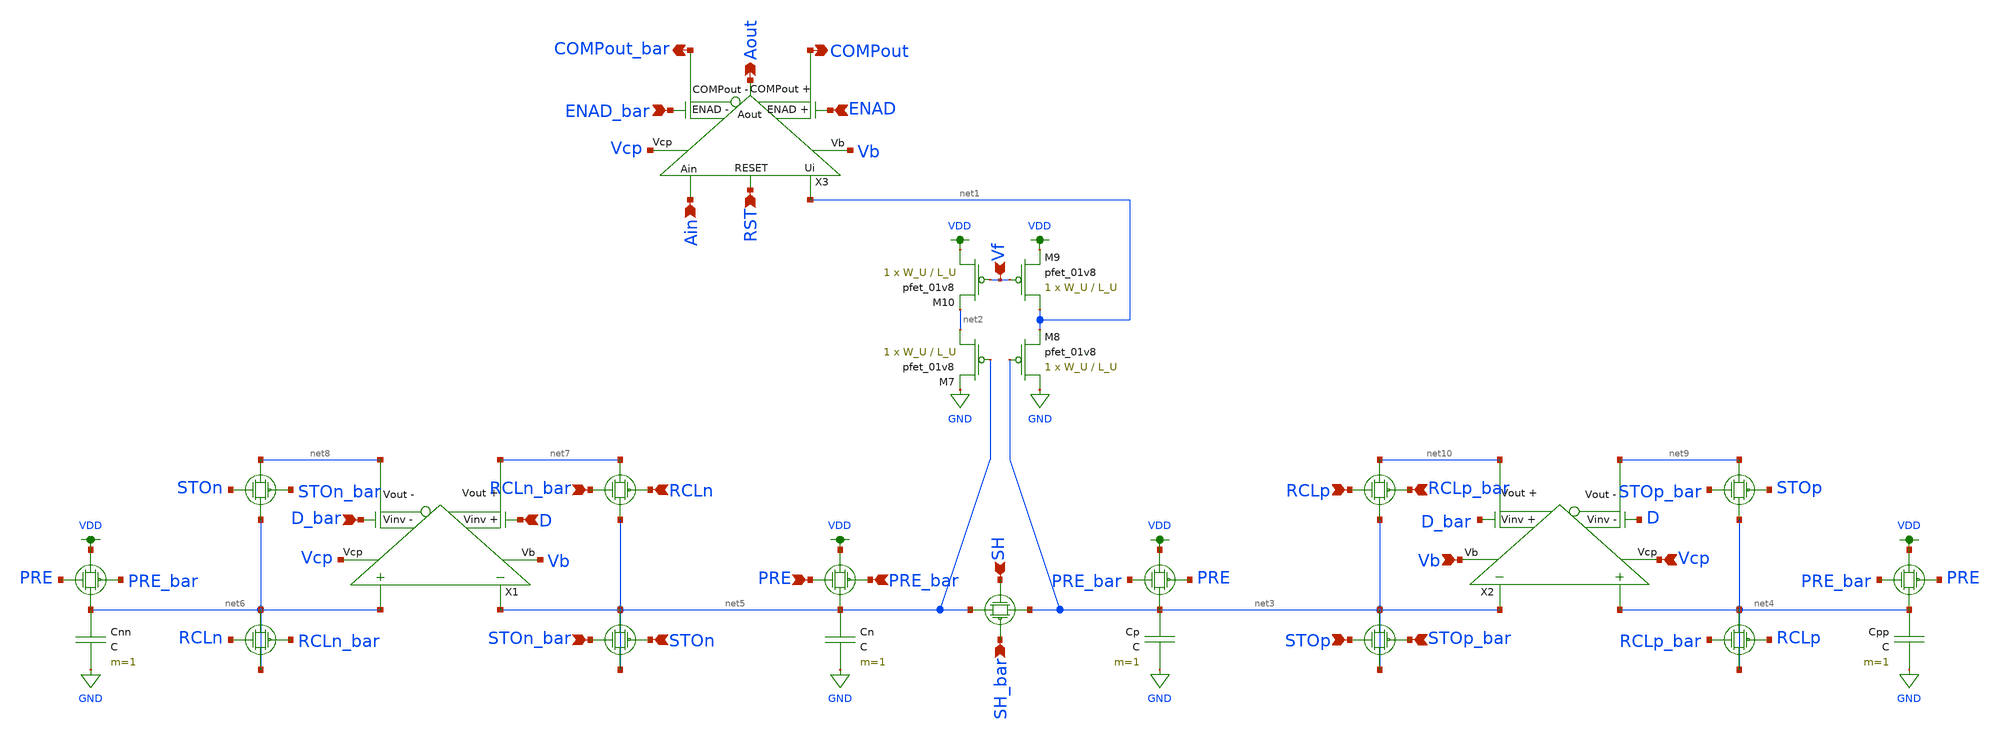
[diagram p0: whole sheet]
** sch_path: schematics/ada_converter.sch
**.subckt ada_converter RCLp STOp RCLp_bar STOp_bar SH SH_bar Vb Vcp RCLn STOn RCLn_bar STOn_bar RST
*+ Ain Aout COMPout_bar COMPout ENAD ENAD_bar Vf PRE_bar PRE D_bar D
*.ipin RCLp
*.ipin STOp
*.ipin RCLp_bar
*.ipin STOp_bar
*.ipin SH
*.ipin SH_bar
*.ipin Vb
*.ipin Vcp
*.ipin RCLn
*.ipin STOn
*.ipin RCLn_bar
*.ipin STOn_bar
*.ipin RST
*.ipin Ain
*.opin Aout
*.opin COMPout_bar
*.opin COMPout
*.ipin ENAD
*.ipin ENAD_bar
*.ipin Vf
*.ipin PRE_bar
*.ipin PRE
*.ipin D_bar
*.ipin D
X1 D_bar net8 net7 Vcp Vb net5 net6 D ota
X2 D net9 net10 Vcp Vb net3 net4 D_bar ota
X3 ENAD_bar COMPout_bar COMPout Vb net1 Ain ENAD Aout Vcp RST comp_pretty
Cp net3 GND C m=1
XM7 net2 net5 GND VDD sky130_fd_pr__pfet_01v8 L=L_U W=W_U nf=1 ad='int((nf+1)/2) * W/nf * 0.29' as='int((nf+2)/2) * W/nf * 0.29'
+ pd='2*int((nf+1)/2) * (W/nf + 0.29)' ps='2*int((nf+2)/2) * (W/nf + 0.29)' nrd='0.29 / W' nrs='0.29 / W'
+ sa=0 sb=0 sd=0 mult=1 m=1
XM8 GND net3 net1 VDD sky130_fd_pr__pfet_01v8 L=L_U W=W_U nf=1 ad='int((nf+1)/2) * W/nf * 0.29' as='int((nf+2)/2) * W/nf * 0.29'
+ pd='2*int((nf+1)/2) * (W/nf + 0.29)' ps='2*int((nf+2)/2) * (W/nf + 0.29)' nrd='0.29 / W' nrs='0.29 / W'
+ sa=0 sb=0 sd=0 mult=1 m=1
XM9 net1 Vf VDD VDD sky130_fd_pr__pfet_01v8 L=L_U W=W_U nf=1 ad='int((nf+1)/2) * W/nf * 0.29' as='int((nf+2)/2) * W/nf * 0.29'
+ pd='2*int((nf+1)/2) * (W/nf + 0.29)' ps='2*int((nf+2)/2) * (W/nf + 0.29)' nrd='0.29 / W' nrs='0.29 / W'
+ sa=0 sb=0 sd=0 mult=1 m=1
XM10 VDD Vf net2 VDD sky130_fd_pr__pfet_01v8 L=L_U W=W_U nf=1 ad='int((nf+1)/2) * W/nf * 0.29' as='int((nf+2)/2) * W/nf * 0.29'
+ pd='2*int((nf+1)/2) * (W/nf + 0.29)' ps='2*int((nf+2)/2) * (W/nf + 0.29)' nrd='0.29 / W' nrs='0.29 / W'
+ sa=0 sb=0 sd=0 mult=1 m=1
Cpp net4 GND C m=1
Cn net5 GND C m=1
Cnn net6 GND C m=1
**.ends

* expanding   symbol:  ./ota.sym # of pins=8
** sym_path: schematics/ota.sym
** sch_path: schematics/ota.sch
.subckt ota Vinv_n Vout_n Vout_p Vcp Vb Vin_n Vin_p Vinv_p
*.ipin Vin_n
*.ipin Vin_p
*.opin Vout_n
*.opin Vout_p
*.ipin Vcp
*.ipin Vb
*.ipin Vinv_p
*.ipin Vinv_n
XM18 net3 net3 VDD VDD sky130_fd_pr__pfet_01v8 L=L_U W=W_U nf=1 ad='int((nf+1)/2) * W/nf * 0.29' as='int((nf+2)/2) * W/nf * 0.29'
+ pd='2*int((nf+1)/2) * (W/nf + 0.29)' ps='2*int((nf+2)/2) * (W/nf + 0.29)' nrd='0.29 / W' nrs='0.29 / W'
+ sa=0 sb=0 sd=0 mult=1 m=1
XM19 net4 Vin_n net1 GND sky130_fd_pr__nfet_01v8 L=L_U W=W_U nf=1 ad='int((nf+1)/2) * W/nf * 0.29' as='int((nf+2)/2) * W/nf * 0.29'
+ pd='2*int((nf+1)/2) * (W/nf + 0.29)' ps='2*int((nf+2)/2) * (W/nf + 0.29)' nrd='0.29 / W' nrs='0.29 / W'
+ sa=0 sb=0 sd=0 mult=1 m=1
XM20 net3 Vin_p net1 GND sky130_fd_pr__nfet_01v8 L=L_U W=W_U nf=1 ad='int((nf+1)/2) * W/nf * 0.29' as='int((nf+2)/2) * W/nf * 0.29'
+ pd='2*int((nf+1)/2) * (W/nf + 0.29)' ps='2*int((nf+2)/2) * (W/nf + 0.29)' nrd='0.29 / W' nrs='0.29 / W'
+ sa=0 sb=0 sd=0 mult=1 m=1
XM21 net1 Vb GND GND sky130_fd_pr__nfet_01v8 L=L_U W=W_U nf=1 ad='int((nf+1)/2) * W/nf * 0.29' as='int((nf+2)/2) * W/nf * 0.29'
+ pd='2*int((nf+1)/2) * (W/nf + 0.29)' ps='2*int((nf+2)/2) * (W/nf + 0.29)' nrd='0.29 / W' nrs='0.29 / W'
+ sa=0 sb=0 sd=0 mult=1 m=1
XM22 net4 net4 VDD VDD sky130_fd_pr__pfet_01v8 L=L_U W=W_U nf=1 ad='int((nf+1)/2) * W/nf * 0.29' as='int((nf+2)/2) * W/nf * 0.29'
+ pd='2*int((nf+1)/2) * (W/nf + 0.29)' ps='2*int((nf+2)/2) * (W/nf + 0.29)' nrd='0.29 / W' nrs='0.29 / W'
+ sa=0 sb=0 sd=0 mult=1 m=1
XM23 net8 net3 VDD VDD sky130_fd_pr__pfet_01v8 L=L_U W=W_U nf=1 ad='int((nf+1)/2) * W/nf * 0.29' as='int((nf+2)/2) * W/nf * 0.29'
+ pd='2*int((nf+1)/2) * (W/nf + 0.29)' ps='2*int((nf+2)/2) * (W/nf + 0.29)' nrd='0.29 / W' nrs='0.29 / W'
+ sa=0 sb=0 sd=0 mult=1 m=1
XM24 net9 net4 VDD VDD sky130_fd_pr__pfet_01v8 L=L_U W=W_U nf=1 ad='int((nf+1)/2) * W/nf * 0.29' as='int((nf+2)/2) * W/nf * 0.29'
+ pd='2*int((nf+1)/2) * (W/nf + 0.29)' ps='2*int((nf+2)/2) * (W/nf + 0.29)' nrd='0.29 / W' nrs='0.29 / W'
+ sa=0 sb=0 sd=0 mult=1 m=1
XM25 net9 Vcp Vout_n VDD sky130_fd_pr__pfet_01v8 L=L_U W=W_U nf=1 ad='int((nf+1)/2) * W/nf * 0.29' as='int((nf+2)/2) * W/nf * 0.29'
+ pd='2*int((nf+1)/2) * (W/nf + 0.29)' ps='2*int((nf+2)/2) * (W/nf + 0.29)' nrd='0.29 / W' nrs='0.29 / W'
+ sa=0 sb=0 sd=0 mult=1 m=1
XM26 Vout_p Vcp net8 VDD sky130_fd_pr__pfet_01v8 L=L_U W=W_U nf=1 ad='int((nf+1)/2) * W/nf * 0.29' as='int((nf+2)/2) * W/nf * 0.29'
+ pd='2*int((nf+1)/2) * (W/nf + 0.29)' ps='2*int((nf+2)/2) * (W/nf + 0.29)' nrd='0.29 / W' nrs='0.29 / W'
+ sa=0 sb=0 sd=0 mult=1 m=1
XM27 Vout_p net7 net5 GND sky130_fd_pr__nfet_01v8 L=L_U W=W_U nf=1 ad='int((nf+1)/2) * W/nf * 0.29' as='int((nf+2)/2) * W/nf * 0.29'
+ pd='2*int((nf+1)/2) * (W/nf + 0.29)' ps='2*int((nf+2)/2) * (W/nf + 0.29)' nrd='0.29 / W' nrs='0.29 / W'
+ sa=0 sb=0 sd=0 mult=1 m=1
XM28 Vout_n net7 net2 GND sky130_fd_pr__nfet_01v8 L=L_U W=W_U nf=1 ad='int((nf+1)/2) * W/nf * 0.29' as='int((nf+2)/2) * W/nf * 0.29'
+ pd='2*int((nf+1)/2) * (W/nf + 0.29)' ps='2*int((nf+2)/2) * (W/nf + 0.29)' nrd='0.29 / W' nrs='0.29 / W'
+ sa=0 sb=0 sd=0 mult=1 m=1
XM29 net5 net6 GND GND sky130_fd_pr__nfet_01v8 L=L_U W=W_U nf=1 ad='int((nf+1)/2) * W/nf * 0.29' as='int((nf+2)/2) * W/nf * 0.29'
+ pd='2*int((nf+1)/2) * (W/nf + 0.29)' ps='2*int((nf+2)/2) * (W/nf + 0.29)' nrd='0.29 / W' nrs='0.29 / W'
+ sa=0 sb=0 sd=0 mult=1 m=1
XM30 net5 Vinv_p net6 GND sky130_fd_pr__nfet_01v8 L=L_U W=W_U nf=1 ad='int((nf+1)/2) * W/nf * 0.29' as='int((nf+2)/2) * W/nf * 0.29'
+ pd='2*int((nf+1)/2) * (W/nf + 0.29)' ps='2*int((nf+2)/2) * (W/nf + 0.29)' nrd='0.29 / W' nrs='0.29 / W'
+ sa=0 sb=0 sd=0 mult=1 m=1
XM31 Vout_p Vinv_p net7 GND sky130_fd_pr__nfet_01v8 L=L_U W=W_U nf=1 ad='int((nf+1)/2) * W/nf * 0.29'
+ as='int((nf+2)/2) * W/nf * 0.29' pd='2*int((nf+1)/2) * (W/nf + 0.29)' ps='2*int((nf+2)/2) * (W/nf + 0.29)'
+ nrd='0.29 / W' nrs='0.29 / W' sa=0 sb=0 sd=0 mult=1 m=1
XM32 net2 net6 GND GND sky130_fd_pr__nfet_01v8 L=L_U W=W_U nf=1 ad='int((nf+1)/2) * W/nf * 0.29' as='int((nf+2)/2) * W/nf * 0.29'
+ pd='2*int((nf+1)/2) * (W/nf + 0.29)' ps='2*int((nf+2)/2) * (W/nf + 0.29)' nrd='0.29 / W' nrs='0.29 / W'
+ sa=0 sb=0 sd=0 mult=1 m=1
XM33 Vout_n Vinv_n net7 GND sky130_fd_pr__nfet_01v8 L=L_U W=W_U nf=1 ad='int((nf+1)/2) * W/nf * 0.29'
+ as='int((nf+2)/2) * W/nf * 0.29' pd='2*int((nf+1)/2) * (W/nf + 0.29)' ps='2*int((nf+2)/2) * (W/nf + 0.29)'
+ nrd='0.29 / W' nrs='0.29 / W' sa=0 sb=0 sd=0 mult=1 m=1
XM34 net2 Vinv_n net6 GND sky130_fd_pr__nfet_01v8 L=L_U W=W_U nf=1 ad='int((nf+1)/2) * W/nf * 0.29' as='int((nf+2)/2) * W/nf * 0.29'
+ pd='2*int((nf+1)/2) * (W/nf + 0.29)' ps='2*int((nf+2)/2) * (W/nf + 0.29)' nrd='0.29 / W' nrs='0.29 / W'
+ sa=0 sb=0 sd=0 mult=1 m=1
.ends


* expanding   symbol:  ./comp_pretty.sym # of pins=10
** sym_path: schematics/comp_pretty.sym
** sch_path: schematics/comp_pretty.sch
.subckt comp_pretty ENAD_n COMPout_n COMPout_p Vb Ui Ain ENAD_p Aout Vcp RST
*.ipin Ain
*.ipin Vcp
*.ipin Vb
*.opin Aout
*.opin COMPout_n
*.opin COMPout_p
*.ipin ENAD_n
*.ipin RST
*.ipin Ui
*.ipin ENAD_p
XM1 net1 net1 VDD VDD sky130_fd_pr__pfet_01v8 L=L_U W=W_U nf=1 ad='int((nf+1)/2) * W/nf * 0.29' as='int((nf+2)/2) * W/nf * 0.29'
+ pd='2*int((nf+1)/2) * (W/nf + 0.29)' ps='2*int((nf+2)/2) * (W/nf + 0.29)' nrd='0.29 / W' nrs='0.29 / W'
+ sa=0 sb=0 sd=0 mult=1 m=1
XM2 net2 Ain net5 GND sky130_fd_pr__nfet_01v8 L=L_U W=W_U nf=1 ad='int((nf+1)/2) * W/nf * 0.29' as='int((nf+2)/2) * W/nf * 0.29'
+ pd='2*int((nf+1)/2) * (W/nf + 0.29)' ps='2*int((nf+2)/2) * (W/nf + 0.29)' nrd='0.29 / W' nrs='0.29 / W'
+ sa=0 sb=0 sd=0 mult=1 m=1
XM3 net1 Ui net5 GND sky130_fd_pr__nfet_01v8 L=L_U W=W_U nf=1 ad='int((nf+1)/2) * W/nf * 0.29' as='int((nf+2)/2) * W/nf * 0.29'
+ pd='2*int((nf+1)/2) * (W/nf + 0.29)' ps='2*int((nf+2)/2) * (W/nf + 0.29)' nrd='0.29 / W' nrs='0.29 / W'
+ sa=0 sb=0 sd=0 mult=1 m=1
XM4 net5 Vb GND GND sky130_fd_pr__nfet_01v8 L=L_U W=W_U nf=1 ad='int((nf+1)/2) * W/nf * 0.29' as='int((nf+2)/2) * W/nf * 0.29'
+ pd='2*int((nf+1)/2) * (W/nf + 0.29)' ps='2*int((nf+2)/2) * (W/nf + 0.29)' nrd='0.29 / W' nrs='0.29 / W'
+ sa=0 sb=0 sd=0 mult=1 m=1
XM5 net2 net2 VDD VDD sky130_fd_pr__pfet_01v8 L=L_U W=W_U nf=1 ad='int((nf+1)/2) * W/nf * 0.29' as='int((nf+2)/2) * W/nf * 0.29'
+ pd='2*int((nf+1)/2) * (W/nf + 0.29)' ps='2*int((nf+2)/2) * (W/nf + 0.29)' nrd='0.29 / W' nrs='0.29 / W'
+ sa=0 sb=0 sd=0 mult=1 m=1
XM6 net8 net1 VDD VDD sky130_fd_pr__pfet_01v8 L=L_U W=W_U nf=1 ad='int((nf+1)/2) * W/nf * 0.29' as='int((nf+2)/2) * W/nf * 0.29'
+ pd='2*int((nf+1)/2) * (W/nf + 0.29)' ps='2*int((nf+2)/2) * (W/nf + 0.29)' nrd='0.29 / W' nrs='0.29 / W'
+ sa=0 sb=0 sd=0 mult=1 m=1
XM7 net9 net2 VDD VDD sky130_fd_pr__pfet_01v8 L=L_U W=W_U nf=1 ad='int((nf+1)/2) * W/nf * 0.29' as='int((nf+2)/2) * W/nf * 0.29'
+ pd='2*int((nf+1)/2) * (W/nf + 0.29)' ps='2*int((nf+2)/2) * (W/nf + 0.29)' nrd='0.29 / W' nrs='0.29 / W'
+ sa=0 sb=0 sd=0 mult=1 m=1
XM8 net9 Vcp COMPout_p VDD sky130_fd_pr__pfet_01v8 L=L_U W=W_U nf=1 ad='int((nf+1)/2) * W/nf * 0.29'
+ as='int((nf+2)/2) * W/nf * 0.29' pd='2*int((nf+1)/2) * (W/nf + 0.29)' ps='2*int((nf+2)/2) * (W/nf + 0.29)'
+ nrd='0.29 / W' nrs='0.29 / W' sa=0 sb=0 sd=0 mult=1 m=1
XM9 COMPout_n Vcp net8 VDD sky130_fd_pr__pfet_01v8 L=L_U W=W_U nf=1 ad='int((nf+1)/2) * W/nf * 0.29'
+ as='int((nf+2)/2) * W/nf * 0.29' pd='2*int((nf+1)/2) * (W/nf + 0.29)' ps='2*int((nf+2)/2) * (W/nf + 0.29)'
+ nrd='0.29 / W' nrs='0.29 / W' sa=0 sb=0 sd=0 mult=1 m=1
XM10 net1 Vb GND GND sky130_fd_pr__nfet_01v8 L=L_U W=W_U nf=1 ad='int((nf+1)/2) * W/nf * 0.29' as='int((nf+2)/2) * W/nf * 0.29'
+ pd='2*int((nf+1)/2) * (W/nf + 0.29)' ps='2*int((nf+2)/2) * (W/nf + 0.29)' nrd='0.29 / W' nrs='0.29 / W'
+ sa=0 sb=0 sd=0 mult=1 m=1
XM11 net2 Vb GND GND sky130_fd_pr__nfet_01v8 L=L_U W=W_U nf=1 ad='int((nf+1)/2) * W/nf * 0.29' as='int((nf+2)/2) * W/nf * 0.29'
+ pd='2*int((nf+1)/2) * (W/nf + 0.29)' ps='2*int((nf+2)/2) * (W/nf + 0.29)' nrd='0.29 / W' nrs='0.29 / W'
+ sa=0 sb=0 sd=0 mult=1 m=1
XM12 COMPout_n net6 net4 GND sky130_fd_pr__nfet_01v8 L=L_U W=W_U nf=1 ad='int((nf+1)/2) * W/nf * 0.29'
+ as='int((nf+2)/2) * W/nf * 0.29' pd='2*int((nf+1)/2) * (W/nf + 0.29)' ps='2*int((nf+2)/2) * (W/nf + 0.29)'
+ nrd='0.29 / W' nrs='0.29 / W' sa=0 sb=0 sd=0 mult=1 m=1
XM13 net6 ENAD_n VDD VDD sky130_fd_pr__pfet_01v8 L=L_U W=W_U nf=1 ad='int((nf+1)/2) * W/nf * 0.29' as='int((nf+2)/2) * W/nf * 0.29'
+ pd='2*int((nf+1)/2) * (W/nf + 0.29)' ps='2*int((nf+2)/2) * (W/nf + 0.29)' nrd='0.29 / W' nrs='0.29 / W'
+ sa=0 sb=0 sd=0 mult=1 m=1
XM14 COMPout_p net6 net3 GND sky130_fd_pr__nfet_01v8 L=L_U W=W_U nf=1 ad='int((nf+1)/2) * W/nf * 0.29'
+ as='int((nf+2)/2) * W/nf * 0.29' pd='2*int((nf+1)/2) * (W/nf + 0.29)' ps='2*int((nf+2)/2) * (W/nf + 0.29)'
+ nrd='0.29 / W' nrs='0.29 / W' sa=0 sb=0 sd=0 mult=1 m=1
XM15 COMPout_p ENAD_n net6 GND sky130_fd_pr__nfet_01v8 L=L_U W=W_U nf=1 ad='int((nf+1)/2) * W/nf * 0.29'
+ as='int((nf+2)/2) * W/nf * 0.29' pd='2*int((nf+1)/2) * (W/nf + 0.29)' ps='2*int((nf+2)/2) * (W/nf + 0.29)'
+ nrd='0.29 / W' nrs='0.29 / W' sa=0 sb=0 sd=0 mult=1 m=1
XM16 net4 net3 GND GND sky130_fd_pr__nfet_01v8 L=L_U W=W_U nf=1 ad='int((nf+1)/2) * W/nf * 0.29' as='int((nf+2)/2) * W/nf * 0.29'
+ pd='2*int((nf+1)/2) * (W/nf + 0.29)' ps='2*int((nf+2)/2) * (W/nf + 0.29)' nrd='0.29 / W' nrs='0.29 / W'
+ sa=0 sb=0 sd=0 mult=1 m=1
XM17 net3 net7 GND GND sky130_fd_pr__nfet_01v8 L=L_U W=W_U nf=1 ad='int((nf+1)/2) * W/nf * 0.29' as='int((nf+2)/2) * W/nf * 0.29'
+ pd='2*int((nf+1)/2) * (W/nf + 0.29)' ps='2*int((nf+2)/2) * (W/nf + 0.29)' nrd='0.29 / W' nrs='0.29 / W'
+ sa=0 sb=0 sd=0 mult=1 m=1
XM18 net7 ENAD_n net3 GND sky130_fd_pr__nfet_01v8 L=L_U W=W_U nf=1 ad='int((nf+1)/2) * W/nf * 0.29' as='int((nf+2)/2) * W/nf * 0.29'
+ pd='2*int((nf+1)/2) * (W/nf + 0.29)' ps='2*int((nf+2)/2) * (W/nf + 0.29)' nrd='0.29 / W' nrs='0.29 / W'
+ sa=0 sb=0 sd=0 mult=1 m=1
XM19 net4 ENAD_p net7 GND sky130_fd_pr__nfet_01v8 L=L_U W=W_U nf=1 ad='int((nf+1)/2) * W/nf * 0.29' as='int((nf+2)/2) * W/nf * 0.29'
+ pd='2*int((nf+1)/2) * (W/nf + 0.29)' ps='2*int((nf+2)/2) * (W/nf + 0.29)' nrd='0.29 / W' nrs='0.29 / W'
+ sa=0 sb=0 sd=0 mult=1 m=1
XM20 net7 RST net3 GND sky130_fd_pr__nfet_01v8 L=L_U W=W_U nf=1 ad='int((nf+1)/2) * W/nf * 0.29' as='int((nf+2)/2) * W/nf * 0.29'
+ pd='2*int((nf+1)/2) * (W/nf + 0.29)' ps='2*int((nf+2)/2) * (W/nf + 0.29)' nrd='0.29 / W' nrs='0.29 / W'
+ sa=0 sb=0 sd=0 mult=1 m=1
C1 net3 GND 0.1p m=1
C2 net7 GND 0.1p m=1
XM26 COMPout_n ENAD_n Aout VDD sky130_fd_pr__pfet_01v8 L=L_U W=W_U nf=1 ad='int((nf+1)/2) * W/nf * 0.29'
+ as='int((nf+2)/2) * W/nf * 0.29' pd='2*int((nf+1)/2) * (W/nf + 0.29)' ps='2*int((nf+2)/2) * (W/nf + 0.29)'
+ nrd='0.29 / W' nrs='0.29 / W' sa=0 sb=0 sd=0 mult=1 m=1
XM27 Aout ENAD_p COMPout_n GND sky130_fd_pr__nfet_01v8 L=L_U W=W_U nf=1 ad='int((nf+1)/2) * W/nf * 0.29'
+ as='int((nf+2)/2) * W/nf * 0.29' pd='2*int((nf+1)/2) * (W/nf + 0.29)' ps='2*int((nf+2)/2) * (W/nf + 0.29)'
+ nrd='0.29 / W' nrs='0.29 / W' sa=0 sb=0 sd=0 mult=1 m=1
.ends

.GLOBAL GND
.GLOBAL VDD
.end
